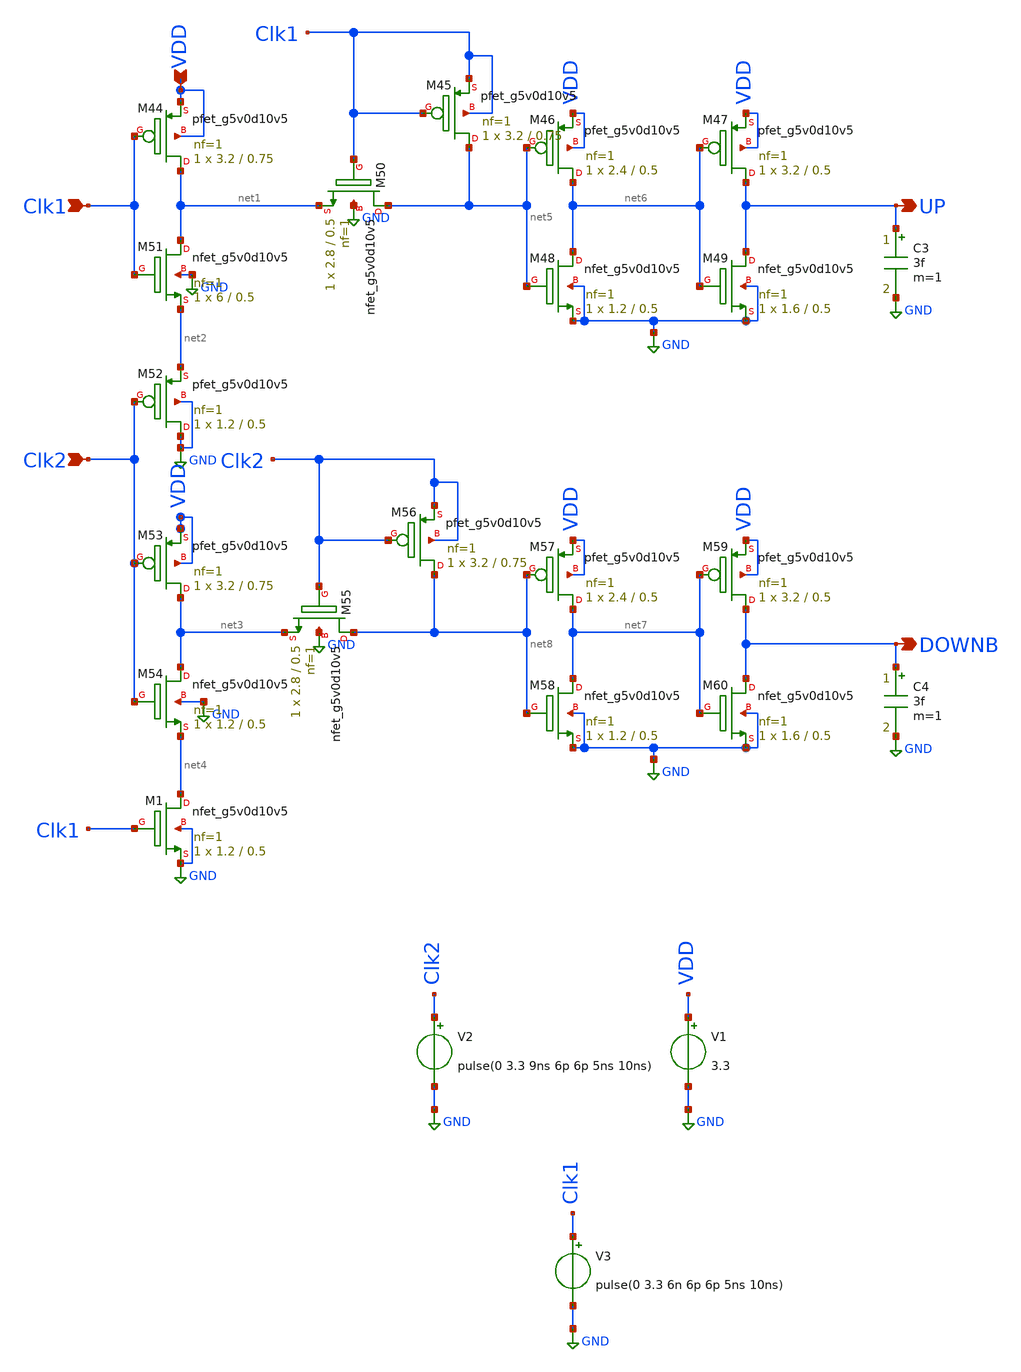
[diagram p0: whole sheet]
** sch_path: Phase-Frequency Detector/PFD_v1.sch
**.subckt PFD_v1 Clk1 Clk2 DOWNB UP VDD
*.ipin Clk1
*.ipin Clk2
*.opin DOWNB
*.opin UP
*.ipin VDD
V1 VDD GND 3.3
V2 Clk2 GND pulse(0 3.3 9ns 6p 6p 5ns 10ns)
V3 Clk1 GND pulse(0 3.3 6n 6p 6p 5ns 10ns)
C3 UP GND 3f m=1
C4 DOWNB GND 3f m=1
XM44 net1 Clk1 VDD VDD sky130_fd_pr__pfet_g5v0d10v5 L=0.75 W=3.2 nf=1 ad='int((nf+1)/2) * W/nf * 0.29'
+ as='int((nf+2)/2) * W/nf * 0.29' pd='2*int((nf+1)/2) * (W/nf + 0.29)' ps='2*int((nf+2)/2) * (W/nf + 0.29)'
+ nrd='0.29 / W' nrs='0.29 / W' sa=0 sb=0 sd=0 mult=1 m=1
XM45 net5 Clk1 Clk1 Clk1 sky130_fd_pr__pfet_g5v0d10v5 L=0.75 W=3.2 nf=1 ad='int((nf+1)/2) * W/nf * 0.29'
+ as='int((nf+2)/2) * W/nf * 0.29' pd='2*int((nf+1)/2) * (W/nf + 0.29)' ps='2*int((nf+2)/2) * (W/nf + 0.29)'
+ nrd='0.29 / W' nrs='0.29 / W' sa=0 sb=0 sd=0 mult=1 m=1
XM46 net6 net5 VDD VDD sky130_fd_pr__pfet_g5v0d10v5 L=0.5 W=2.4 nf=1 ad='int((nf+1)/2) * W/nf * 0.29'
+ as='int((nf+2)/2) * W/nf * 0.29' pd='2*int((nf+1)/2) * (W/nf + 0.29)' ps='2*int((nf+2)/2) * (W/nf + 0.29)'
+ nrd='0.29 / W' nrs='0.29 / W' sa=0 sb=0 sd=0 mult=1 m=1
XM47 UP net6 VDD VDD sky130_fd_pr__pfet_g5v0d10v5 L=0.5 W=3.2 nf=1 ad='int((nf+1)/2) * W/nf * 0.29' as='int((nf+2)/2) * W/nf * 0.29'
+ pd='2*int((nf+1)/2) * (W/nf + 0.29)' ps='2*int((nf+2)/2) * (W/nf + 0.29)' nrd='0.29 / W' nrs='0.29 / W'
+ sa=0 sb=0 sd=0 mult=1 m=1
XM48 net6 net5 GND GND sky130_fd_pr__nfet_g5v0d10v5 L=0.5 W=1.2 nf=1 ad='int((nf+1)/2) * W/nf * 0.29'
+ as='int((nf+2)/2) * W/nf * 0.29' pd='2*int((nf+1)/2) * (W/nf + 0.29)' ps='2*int((nf+2)/2) * (W/nf + 0.29)'
+ nrd='0.29 / W' nrs='0.29 / W' sa=0 sb=0 sd=0 mult=1 m=1
XM49 UP net6 GND GND sky130_fd_pr__nfet_g5v0d10v5 L=0.5 W=1.6 nf=1 ad='int((nf+1)/2) * W/nf * 0.29' as='int((nf+2)/2) * W/nf * 0.29'
+ pd='2*int((nf+1)/2) * (W/nf + 0.29)' ps='2*int((nf+2)/2) * (W/nf + 0.29)' nrd='0.29 / W' nrs='0.29 / W'
+ sa=0 sb=0 sd=0 mult=1 m=1
XM50 net5 Clk1 net1 GND sky130_fd_pr__nfet_g5v0d10v5 L=0.5 W=2.8 nf=1 ad='int((nf+1)/2) * W/nf * 0.29'
+ as='int((nf+2)/2) * W/nf * 0.29' pd='2*int((nf+1)/2) * (W/nf + 0.29)' ps='2*int((nf+2)/2) * (W/nf + 0.29)'
+ nrd='0.29 / W' nrs='0.29 / W' sa=0 sb=0 sd=0 mult=1 m=1
XM51 net1 Clk1 net2 GND sky130_fd_pr__nfet_g5v0d10v5 L=0.5 W=6 nf=1 ad='int((nf+1)/2) * W/nf * 0.29'
+ as='int((nf+2)/2) * W/nf * 0.29' pd='2*int((nf+1)/2) * (W/nf + 0.29)' ps='2*int((nf+2)/2) * (W/nf + 0.29)'
+ nrd='0.29 / W' nrs='0.29 / W' sa=0 sb=0 sd=0 mult=1 m=1
XM52 GND Clk2 net2 GND sky130_fd_pr__pfet_g5v0d10v5 L=0.5 W=1.2 nf=1 ad='int((nf+1)/2) * W/nf * 0.29'
+ as='int((nf+2)/2) * W/nf * 0.29' pd='2*int((nf+1)/2) * (W/nf + 0.29)' ps='2*int((nf+2)/2) * (W/nf + 0.29)'
+ nrd='0.29 / W' nrs='0.29 / W' sa=0 sb=0 sd=0 mult=1 m=1
XM53 net3 Clk2 VDD VDD sky130_fd_pr__pfet_g5v0d10v5 L=0.75 W=3.2 nf=1 ad='int((nf+1)/2) * W/nf * 0.29'
+ as='int((nf+2)/2) * W/nf * 0.29' pd='2*int((nf+1)/2) * (W/nf + 0.29)' ps='2*int((nf+2)/2) * (W/nf + 0.29)'
+ nrd='0.29 / W' nrs='0.29 / W' sa=0 sb=0 sd=0 mult=1 m=1
XM54 net3 Clk2 net4 GND sky130_fd_pr__nfet_g5v0d10v5 L=0.5 W=1.2 nf=1 ad='int((nf+1)/2) * W/nf * 0.29'
+ as='int((nf+2)/2) * W/nf * 0.29' pd='2*int((nf+1)/2) * (W/nf + 0.29)' ps='2*int((nf+2)/2) * (W/nf + 0.29)'
+ nrd='0.29 / W' nrs='0.29 / W' sa=0 sb=0 sd=0 mult=1 m=1
XM55 net8 Clk2 net3 GND sky130_fd_pr__nfet_g5v0d10v5 L=0.5 W=2.8 nf=1 ad='int((nf+1)/2) * W/nf * 0.29'
+ as='int((nf+2)/2) * W/nf * 0.29' pd='2*int((nf+1)/2) * (W/nf + 0.29)' ps='2*int((nf+2)/2) * (W/nf + 0.29)'
+ nrd='0.29 / W' nrs='0.29 / W' sa=0 sb=0 sd=0 mult=1 m=1
XM56 net8 Clk2 Clk2 Clk2 sky130_fd_pr__pfet_g5v0d10v5 L=0.75 W=3.2 nf=1 ad='int((nf+1)/2) * W/nf * 0.29'
+ as='int((nf+2)/2) * W/nf * 0.29' pd='2*int((nf+1)/2) * (W/nf + 0.29)' ps='2*int((nf+2)/2) * (W/nf + 0.29)'
+ nrd='0.29 / W' nrs='0.29 / W' sa=0 sb=0 sd=0 mult=1 m=1
XM57 net7 net8 VDD VDD sky130_fd_pr__pfet_g5v0d10v5 L=0.5 W=2.4 nf=1 ad='int((nf+1)/2) * W/nf * 0.29'
+ as='int((nf+2)/2) * W/nf * 0.29' pd='2*int((nf+1)/2) * (W/nf + 0.29)' ps='2*int((nf+2)/2) * (W/nf + 0.29)'
+ nrd='0.29 / W' nrs='0.29 / W' sa=0 sb=0 sd=0 mult=1 m=1
XM58 net7 net8 GND GND sky130_fd_pr__nfet_g5v0d10v5 L=0.5 W=1.2 nf=1 ad='int((nf+1)/2) * W/nf * 0.29'
+ as='int((nf+2)/2) * W/nf * 0.29' pd='2*int((nf+1)/2) * (W/nf + 0.29)' ps='2*int((nf+2)/2) * (W/nf + 0.29)'
+ nrd='0.29 / W' nrs='0.29 / W' sa=0 sb=0 sd=0 mult=1 m=1
XM59 DOWNB net7 VDD VDD sky130_fd_pr__pfet_g5v0d10v5 L=0.5 W=3.2 nf=1 ad='int((nf+1)/2) * W/nf * 0.29'
+ as='int((nf+2)/2) * W/nf * 0.29' pd='2*int((nf+1)/2) * (W/nf + 0.29)' ps='2*int((nf+2)/2) * (W/nf + 0.29)'
+ nrd='0.29 / W' nrs='0.29 / W' sa=0 sb=0 sd=0 mult=1 m=1
XM60 DOWNB net7 GND GND sky130_fd_pr__nfet_g5v0d10v5 L=0.5 W=1.6 nf=1 ad='int((nf+1)/2) * W/nf * 0.29'
+ as='int((nf+2)/2) * W/nf * 0.29' pd='2*int((nf+1)/2) * (W/nf + 0.29)' ps='2*int((nf+2)/2) * (W/nf + 0.29)'
+ nrd='0.29 / W' nrs='0.29 / W' sa=0 sb=0 sd=0 mult=1 m=1
XM1 net4 Clk1 GND GND sky130_fd_pr__nfet_g5v0d10v5 L=0.5 W=1.2 nf=1 ad='int((nf+1)/2) * W/nf * 0.29'
+ as='int((nf+2)/2) * W/nf * 0.29' pd='2*int((nf+1)/2) * (W/nf + 0.29)' ps='2*int((nf+2)/2) * (W/nf + 0.29)'
+ nrd='0.29 / W' nrs='0.29 / W' sa=0 sb=0 sd=0 mult=1 m=1
**** begin user architecture code


.include /home/huydq/pdk/sky130A/libs.ref/sky130_fd_sc_hd/spice/sky130_fd_sc_hd.spice

.control
save all
tran 1n 100n
write testtiep.raw
.endc

.lib $::SKYWATER_MODELS/sky130.lib.spice tt
**** end user architecture code
**.ends
.GLOBAL GND
.end
